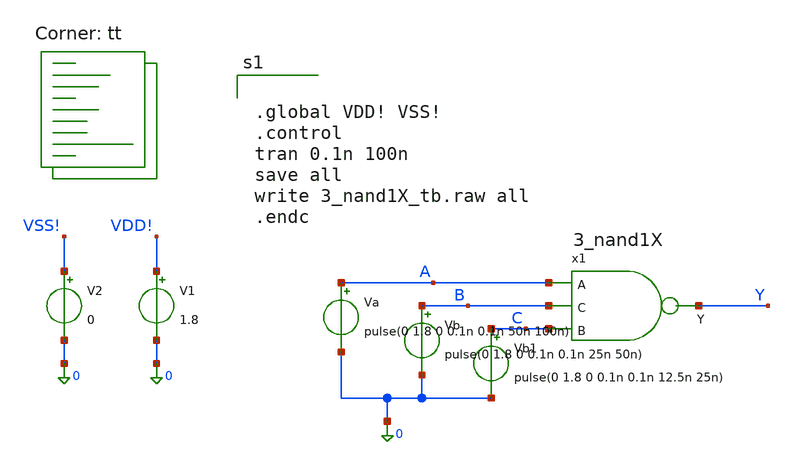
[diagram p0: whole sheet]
** sch_path: 3_nand1X/3_nand1X_tb.sch
**.subckt 3_nand1X_tb
V1 VDD! 0 1.8
Va A 0 pulse(0 1.8 0 0.1n 0.1n 50n 100n)
Vb B 0 pulse(0 1.8 0 0.1n 0.1n 25n 50n)
V2 VSS! 0 0
x1 A B C Y 3_nand1X
Vb1 C 0 pulse(0 1.8 0 0.1n 0.1n 12.5n 25n)
**** begin user architecture code
.lib $::SKYWATER_MODELS/sky130.lib.spice tt


.global VDD! VSS!
.control
tran 0.1n 100n
save all
write 3_nand1X_tb.raw all
.endc


**** end user architecture code
**.ends

* expanding   symbol:  /foss/designs/micron/micron_stdcells/3_nand1X/3_nand1X.sym # of pins=4
** sym_path: 3_nand1X/3_nand1X.sym
** sch_path: 3_nand1X/3_nand1X.sch
.subckt 3_nand1X A C B Y
*.ipin A
*.ipin B
*.ipin C
*.opin Y
XM1 Y A VDD! VDD! sky130_fd_pr__pfet_01v8 L=0.15 W=0.63 nf=1 ad='int((1 + 1)/2) * 0.63 / 1 * 0.29' as='int((1 + 2)/2) * 0.63 / 1 * 0.29'
+ pd='2*int((1 + 1)/2) * (0.63 / 1 + 0.29)' ps='2*int((1 + 2)/2) * (0.63 / 1 + 0.29)' nrd='0.29 / 0.63 '
+ nrs='0.29 / 0.63 ' sa=0 sb=0 sd=0 mult=2 m=2
XM2 Y A net1 VSS! sky130_fd_pr__nfet_01v8 L=0.15 W=0.42 nf=1 ad='int((1 + 1)/2) * 0.42 / 1 * 0.29' as='int((1 + 2)/2) * 0.42 / 1 * 0.29'
+ pd='2*int((1 + 1)/2) * (0.42 / 1 + 0.29)' ps='2*int((1 + 2)/2) * (0.42 / 1 + 0.29)' nrd='0.29 / 0.42 '
+ nrs='0.29 / 0.42 ' sa=0 sb=0 sd=0 mult=1 m=1
XM5 net1 B net2 VSS! sky130_fd_pr__nfet_01v8 L=0.15 W=0.42 nf=1 ad='int((1 + 1)/2) * 0.42 / 1 * 0.29'
+ as='int((1 + 2)/2) * 0.42 / 1 * 0.29' pd='2*int((1 + 1)/2) * (0.42 / 1 + 0.29)' ps='2*int((1 + 2)/2) * (0.42 / 1 + 0.29)'
+ nrd='0.29 / 0.42 ' nrs='0.29 / 0.42 ' sa=0 sb=0 sd=0 mult=1 m=1
XM6 net2 C VSS! VSS! sky130_fd_pr__nfet_01v8 L=0.15 W=0.42 nf=1 ad='int((1 + 1)/2) * 0.42 / 1 * 0.29'
+ as='int((1 + 2)/2) * 0.42 / 1 * 0.29' pd='2*int((1 + 1)/2) * (0.42 / 1 + 0.29)' ps='2*int((1 + 2)/2) * (0.42 / 1 + 0.29)'
+ nrd='0.29 / 0.42 ' nrs='0.29 / 0.42 ' sa=0 sb=0 sd=0 mult=1 m=1
XM3 Y B VDD! VDD! sky130_fd_pr__pfet_01v8 L=0.15 W=0.63 nf=1 ad='int((1 + 1)/2) * 0.63 / 1 * 0.29' as='int((1 + 2)/2) * 0.63 / 1 * 0.29'
+ pd='2*int((1 + 1)/2) * (0.63 / 1 + 0.29)' ps='2*int((1 + 2)/2) * (0.63 / 1 + 0.29)' nrd='0.29 / 0.63 '
+ nrs='0.29 / 0.63 ' sa=0 sb=0 sd=0 mult=2 m=2
XM4 Y C VDD! VDD! sky130_fd_pr__pfet_01v8 L=0.15 W=0.63 nf=1 ad='int((1 + 1)/2) * 0.63 / 1 * 0.29' as='int((1 + 2)/2) * 0.63 / 1 * 0.29'
+ pd='2*int((1 + 1)/2) * (0.63 / 1 + 0.29)' ps='2*int((1 + 2)/2) * (0.63 / 1 + 0.29)' nrd='0.29 / 0.63 '
+ nrs='0.29 / 0.63 ' sa=0 sb=0 sd=0 mult=2 m=2
.ends

.end
